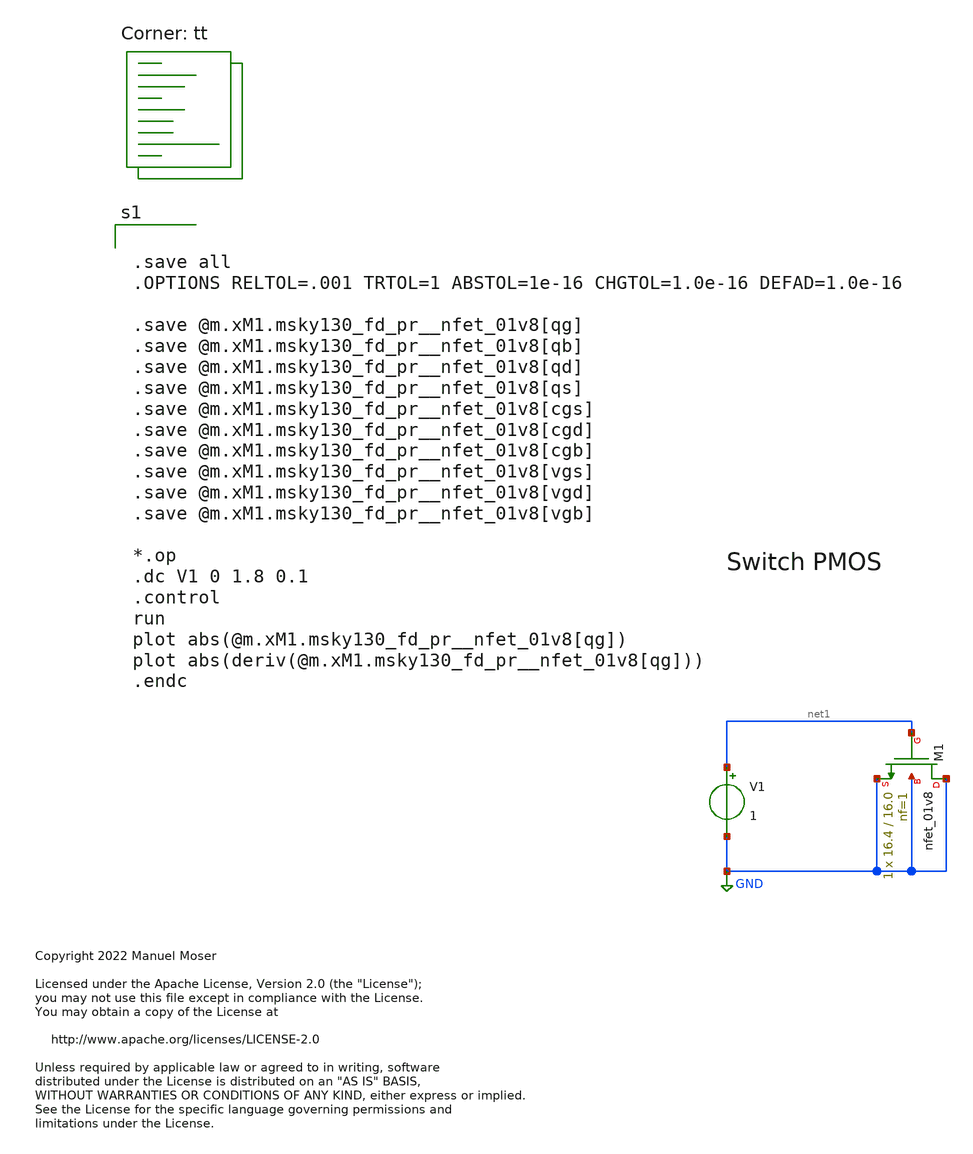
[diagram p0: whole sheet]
** sch_path: archive/xschem/adc_noise_decoup_cell/cgsd_cell1.sch
* Copyright 2022 Manuel Moser
* Licensed under the Apache License, Version 2.0 (the "License");
**.subckt cgsd_cell1
V1 net1 GND 1
XM1 GND net1 GND GND sky130_fd_pr__nfet_01v8 L=16.0 W=16.4 nf=1 ad='int((nf+1)/2) * W/nf * 0.29' as='int((nf+2)/2) * W/nf * 0.29'
+ pd='2*int((nf+1)/2) * (W/nf + 0.29)' ps='2*int((nf+2)/2) * (W/nf + 0.29)' nrd='0.29 / W' nrs='0.29 / W'
+ sa=0 sb=0 sd=0 mult=1 m=1
**** begin user architecture code


.save all
.OPTIONS RELTOL=.001 TRTOL=1 ABSTOL=1e-16 CHGTOL=1.0e-16 DEFAD=1.0e-16

.save @m.xM1.msky130_fd_pr__nfet_01v8[qg]
.save @m.xM1.msky130_fd_pr__nfet_01v8[qb]
.save @m.xM1.msky130_fd_pr__nfet_01v8[qd]
.save @m.xM1.msky130_fd_pr__nfet_01v8[qs]
.save @m.xM1.msky130_fd_pr__nfet_01v8[cgs]
.save @m.xM1.msky130_fd_pr__nfet_01v8[cgd]
.save @m.xM1.msky130_fd_pr__nfet_01v8[cgb]
.save @m.xM1.msky130_fd_pr__nfet_01v8[vgs]
.save @m.xM1.msky130_fd_pr__nfet_01v8[vgd]
.save @m.xM1.msky130_fd_pr__nfet_01v8[vgb]

*.op
.dc V1 0 1.8 0.1
.control
run
plot abs(@m.xM1.msky130_fd_pr__nfet_01v8[qg])
plot abs(deriv(@m.xM1.msky130_fd_pr__nfet_01v8[qg]))
.endc



.lib $::SKYWATER_MODELS/sky130.lib.spice tt
**** end user architecture code
**.ends
.GLOBAL GND
.end
